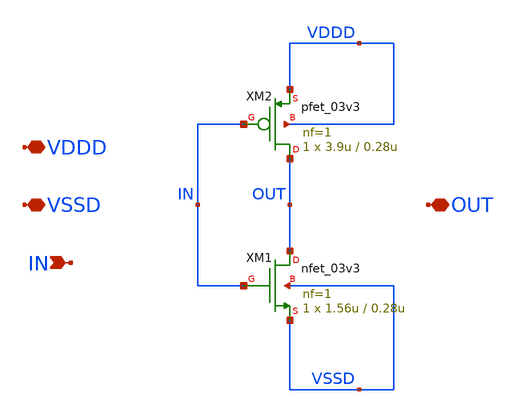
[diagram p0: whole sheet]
** sch_path: SAR_ADC/Dynamic_Comparator/xschem/Dynamic_Comparator_inv_1x.sch
**.subckt Dynamic_Comparator_inv_1x VDDD VSSD IN OUT
*.iopin VDDD
*.iopin VSSD
*.ipin IN
*.iopin OUT
XM1 OUT IN VSSD VSSD nfet_03v3 L=0.28u W=1.56u nf=1 ad='int((nf+1)/2) * W/nf * 0.18u' as='int((nf+2)/2) * W/nf * 0.18u'
+ pd='2*int((nf+1)/2) * (W/nf + 0.18u)' ps='2*int((nf+2)/2) * (W/nf + 0.18u)' nrd='0.18u / W' nrs='0.18u / W'
+ sa=0 sb=0 sd=0 m=1
XM2 OUT IN VDDD VDDD pfet_03v3 L=0.28u W=3.9u nf=1 ad='int((nf+1)/2) * W/nf * 0.18u' as='int((nf+2)/2) * W/nf * 0.18u'
+ pd='2*int((nf+1)/2) * (W/nf + 0.18u)' ps='2*int((nf+2)/2) * (W/nf + 0.18u)' nrd='0.18u / W' nrs='0.18u / W'
+ sa=0 sb=0 sd=0 m=1
**.ends
.end
